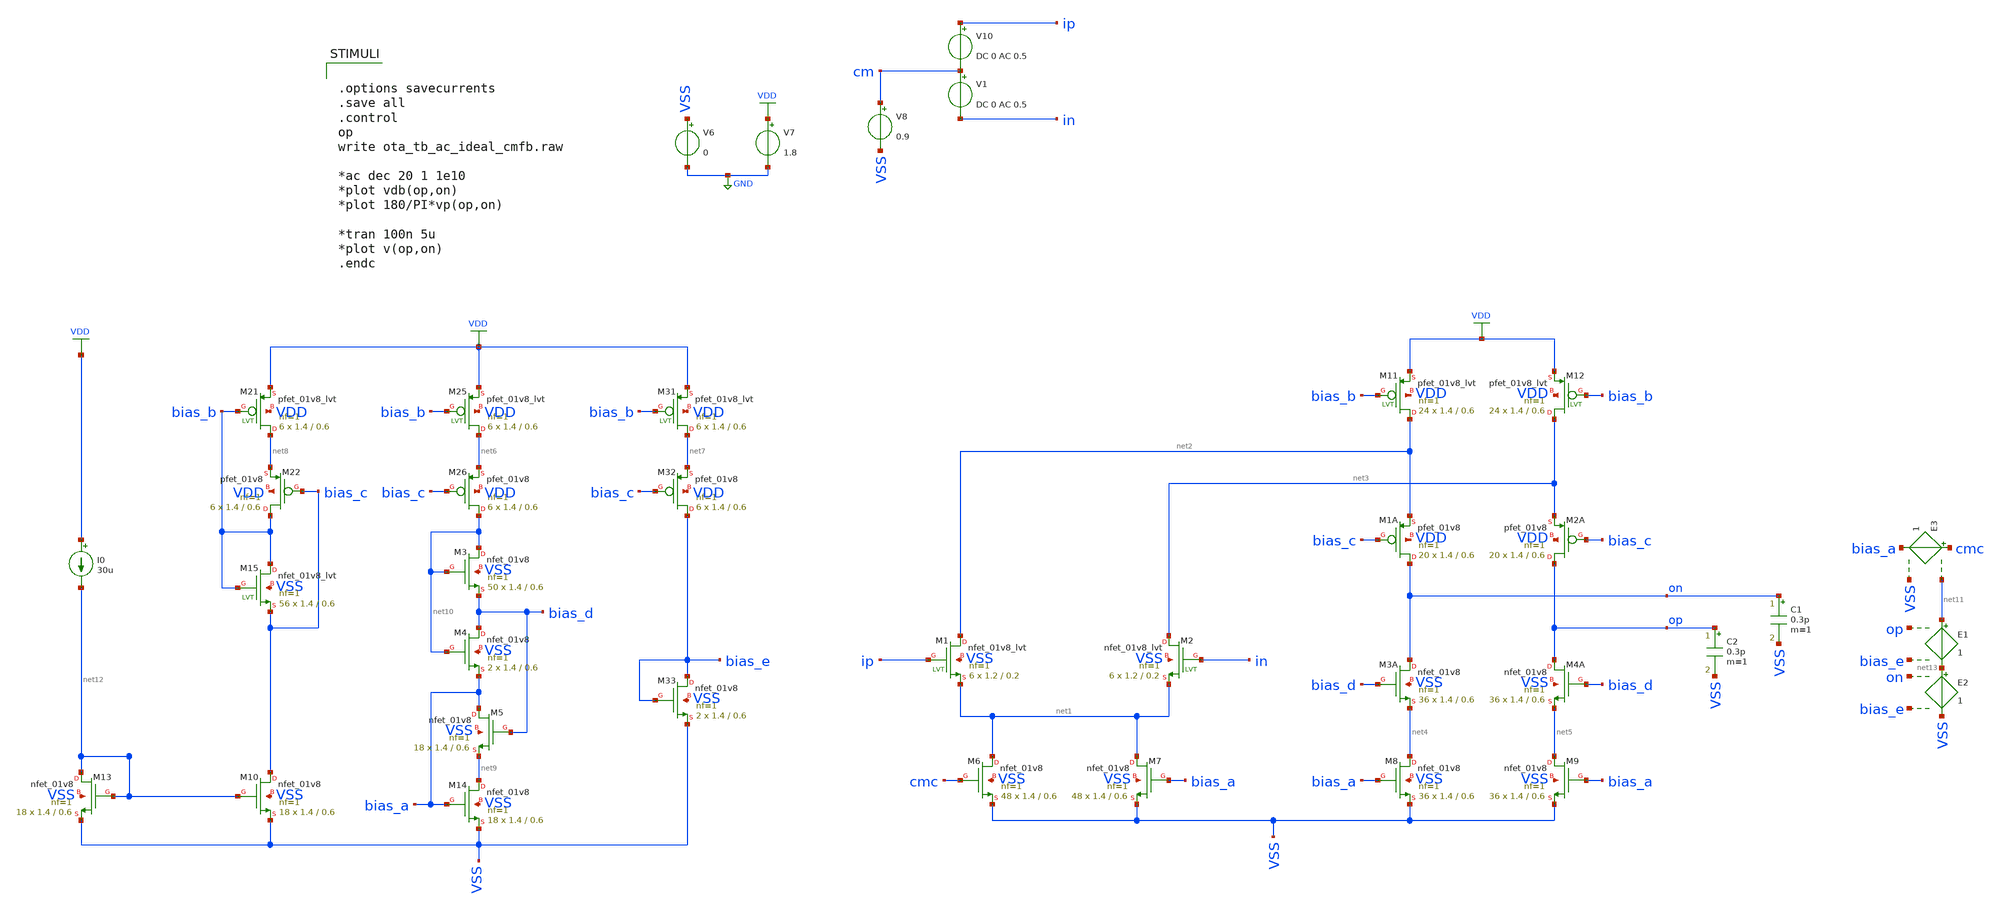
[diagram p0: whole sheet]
** sch_path: verification/schematic/folded_cascode_tb.sch
**.subckt folded_cascode_tb
XM1 net2 ip net1 VSS sky130_fd_pr__nfet_01v8_lvt L=0.2 W=1.2 nf=1 ad='int((nf+1)/2) * W/nf * 0.29' as='int((nf+2)/2) * W/nf * 0.29'
+ pd='2*int((nf+1)/2) * (W/nf + 0.29)' ps='2*int((nf+2)/2) * (W/nf + 0.29)' nrd='0.29 / W' nrs='0.29 / W'
+ sa=0 sb=0 sd=0 mult=6 m=6
XM2 net3 in net1 VSS sky130_fd_pr__nfet_01v8_lvt L=0.2 W=1.2 nf=1 ad='int((nf+1)/2) * W/nf * 0.29' as='int((nf+2)/2) * W/nf * 0.29'
+ pd='2*int((nf+1)/2) * (W/nf + 0.29)' ps='2*int((nf+2)/2) * (W/nf + 0.29)' nrd='0.29 / W' nrs='0.29 / W'
+ sa=0 sb=0 sd=0 mult=6 m=6
XM6 net1 cmc VSS VSS sky130_fd_pr__nfet_01v8 L=0.6 W=1.4 nf=1 ad='int((nf+1)/2) * W/nf * 0.29' as='int((nf+2)/2) * W/nf * 0.29'
+ pd='2*int((nf+1)/2) * (W/nf + 0.29)' ps='2*int((nf+2)/2) * (W/nf + 0.29)' nrd='0.29 / W' nrs='0.29 / W'
+ sa=0 sb=0 sd=0 mult=48 m=48
XM7 net1 bias_a VSS VSS sky130_fd_pr__nfet_01v8 L=0.6 W=1.4 nf=1 ad='int((nf+1)/2) * W/nf * 0.29' as='int((nf+2)/2) * W/nf * 0.29'
+ pd='2*int((nf+1)/2) * (W/nf + 0.29)' ps='2*int((nf+2)/2) * (W/nf + 0.29)' nrd='0.29 / W' nrs='0.29 / W'
+ sa=0 sb=0 sd=0 mult=48 m=48
XM11 net2 bias_b VDD VDD sky130_fd_pr__pfet_01v8_lvt L=0.6 W=1.4 nf=1 ad='int((nf+1)/2) * W/nf * 0.29'
+ as='int((nf+2)/2) * W/nf * 0.29' pd='2*int((nf+1)/2) * (W/nf + 0.29)' ps='2*int((nf+2)/2) * (W/nf + 0.29)'
+ nrd='0.29 / W' nrs='0.29 / W' sa=0 sb=0 sd=0 mult=24 m=24
XM12 net3 bias_b VDD VDD sky130_fd_pr__pfet_01v8_lvt L=0.6 W=1.4 nf=1 ad='int((nf+1)/2) * W/nf * 0.29'
+ as='int((nf+2)/2) * W/nf * 0.29' pd='2*int((nf+1)/2) * (W/nf + 0.29)' ps='2*int((nf+2)/2) * (W/nf + 0.29)'
+ nrd='0.29 / W' nrs='0.29 / W' sa=0 sb=0 sd=0 mult=24 m=24
XM1A on bias_c net2 VDD sky130_fd_pr__pfet_01v8 L=0.6 W=1.4 nf=1 ad='int((nf+1)/2) * W/nf * 0.29' as='int((nf+2)/2) * W/nf * 0.29'
+ pd='2*int((nf+1)/2) * (W/nf + 0.29)' ps='2*int((nf+2)/2) * (W/nf + 0.29)' nrd='0.29 / W' nrs='0.29 / W'
+ sa=0 sb=0 sd=0 mult=20 m=20
XM2A op bias_c net3 VDD sky130_fd_pr__pfet_01v8 L=0.6 W=1.4 nf=1 ad='int((nf+1)/2) * W/nf * 0.29' as='int((nf+2)/2) * W/nf * 0.29'
+ pd='2*int((nf+1)/2) * (W/nf + 0.29)' ps='2*int((nf+2)/2) * (W/nf + 0.29)' nrd='0.29 / W' nrs='0.29 / W'
+ sa=0 sb=0 sd=0 mult=20 m=20
XM3A on bias_d net4 VSS sky130_fd_pr__nfet_01v8 L=0.6 W=1.4 nf=1 ad='int((nf+1)/2) * W/nf * 0.29' as='int((nf+2)/2) * W/nf * 0.29'
+ pd='2*int((nf+1)/2) * (W/nf + 0.29)' ps='2*int((nf+2)/2) * (W/nf + 0.29)' nrd='0.29 / W' nrs='0.29 / W'
+ sa=0 sb=0 sd=0 mult=36 m=36
XM4A op bias_d net5 VSS sky130_fd_pr__nfet_01v8 L=0.6 W=1.4 nf=1 ad='int((nf+1)/2) * W/nf * 0.29' as='int((nf+2)/2) * W/nf * 0.29'
+ pd='2*int((nf+1)/2) * (W/nf + 0.29)' ps='2*int((nf+2)/2) * (W/nf + 0.29)' nrd='0.29 / W' nrs='0.29 / W'
+ sa=0 sb=0 sd=0 mult=36 m=36
XM8 net4 bias_a VSS VSS sky130_fd_pr__nfet_01v8 L=0.6 W=1.4 nf=1 ad='int((nf+1)/2) * W/nf * 0.29' as='int((nf+2)/2) * W/nf * 0.29'
+ pd='2*int((nf+1)/2) * (W/nf + 0.29)' ps='2*int((nf+2)/2) * (W/nf + 0.29)' nrd='0.29 / W' nrs='0.29 / W'
+ sa=0 sb=0 sd=0 mult=36 m=36
XM9 net5 bias_a VSS VSS sky130_fd_pr__nfet_01v8 L=0.6 W=1.4 nf=1 ad='int((nf+1)/2) * W/nf * 0.29' as='int((nf+2)/2) * W/nf * 0.29'
+ pd='2*int((nf+1)/2) * (W/nf + 0.29)' ps='2*int((nf+2)/2) * (W/nf + 0.29)' nrd='0.29 / W' nrs='0.29 / W'
+ sa=0 sb=0 sd=0 mult=36 m=36
V6 VSS GND 0
V7 VDD GND 1.8
V8 cm VSS 0.9
V10 ip cm DC 0 AC 0.5
V1 cm in DC 0 AC 0.5
XM22 bias_b bias_c net8 VDD sky130_fd_pr__pfet_01v8 L=0.6 W=1.4 nf=1 ad='int((nf+1)/2) * W/nf * 0.29'
+ as='int((nf+2)/2) * W/nf * 0.29' pd='2*int((nf+1)/2) * (W/nf + 0.29)' ps='2*int((nf+2)/2) * (W/nf + 0.29)'
+ nrd='0.29 / W' nrs='0.29 / W' sa=0 sb=0 sd=0 mult=6 m=6
XM26 net10 bias_c net6 VDD sky130_fd_pr__pfet_01v8 L=0.6 W=1.4 nf=1 ad='int((nf+1)/2) * W/nf * 0.29'
+ as='int((nf+2)/2) * W/nf * 0.29' pd='2*int((nf+1)/2) * (W/nf + 0.29)' ps='2*int((nf+2)/2) * (W/nf + 0.29)'
+ nrd='0.29 / W' nrs='0.29 / W' sa=0 sb=0 sd=0 mult=6 m=6
XM32 bias_e bias_c net7 VDD sky130_fd_pr__pfet_01v8 L=0.6 W=1.4 nf=1 ad='int((nf+1)/2) * W/nf * 0.29'
+ as='int((nf+2)/2) * W/nf * 0.29' pd='2*int((nf+1)/2) * (W/nf + 0.29)' ps='2*int((nf+2)/2) * (W/nf + 0.29)'
+ nrd='0.29 / W' nrs='0.29 / W' sa=0 sb=0 sd=0 mult=6 m=6
XM33 bias_e bias_e VSS VSS sky130_fd_pr__nfet_01v8 L=0.6 W=1.4 nf=1 ad='int((nf+1)/2) * W/nf * 0.29'
+ as='int((nf+2)/2) * W/nf * 0.29' pd='2*int((nf+1)/2) * (W/nf + 0.29)' ps='2*int((nf+2)/2) * (W/nf + 0.29)'
+ nrd='0.29 / W' nrs='0.29 / W' sa=0 sb=0 sd=0 mult=2 m=2
XM21 net8 bias_b VDD VDD sky130_fd_pr__pfet_01v8_lvt L=0.6 W=1.4 nf=1 ad='int((nf+1)/2) * W/nf * 0.29'
+ as='int((nf+2)/2) * W/nf * 0.29' pd='2*int((nf+1)/2) * (W/nf + 0.29)' ps='2*int((nf+2)/2) * (W/nf + 0.29)'
+ nrd='0.29 / W' nrs='0.29 / W' sa=0 sb=0 sd=0 mult=6 m=6
XM25 net6 bias_b VDD VDD sky130_fd_pr__pfet_01v8_lvt L=0.6 W=1.4 nf=1 ad='int((nf+1)/2) * W/nf * 0.29'
+ as='int((nf+2)/2) * W/nf * 0.29' pd='2*int((nf+1)/2) * (W/nf + 0.29)' ps='2*int((nf+2)/2) * (W/nf + 0.29)'
+ nrd='0.29 / W' nrs='0.29 / W' sa=0 sb=0 sd=0 mult=6 m=6
XM31 net7 bias_b VDD VDD sky130_fd_pr__pfet_01v8_lvt L=0.6 W=1.4 nf=1 ad='int((nf+1)/2) * W/nf * 0.29'
+ as='int((nf+2)/2) * W/nf * 0.29' pd='2*int((nf+1)/2) * (W/nf + 0.29)' ps='2*int((nf+2)/2) * (W/nf + 0.29)'
+ nrd='0.29 / W' nrs='0.29 / W' sa=0 sb=0 sd=0 mult=6 m=6
XM3 net10 net10 bias_d VSS sky130_fd_pr__nfet_01v8 L=0.6 W=1.4 nf=1 ad='int((nf+1)/2) * W/nf * 0.29'
+ as='int((nf+2)/2) * W/nf * 0.29' pd='2*int((nf+1)/2) * (W/nf + 0.29)' ps='2*int((nf+2)/2) * (W/nf + 0.29)'
+ nrd='0.29 / W' nrs='0.29 / W' sa=0 sb=0 sd=0 mult=50 m=50
XM4 bias_d net10 bias_a VSS sky130_fd_pr__nfet_01v8 L=0.6 W=1.4 nf=1 ad='int((nf+1)/2) * W/nf * 0.29'
+ as='int((nf+2)/2) * W/nf * 0.29' pd='2*int((nf+1)/2) * (W/nf + 0.29)' ps='2*int((nf+2)/2) * (W/nf + 0.29)'
+ nrd='0.29 / W' nrs='0.29 / W' sa=0 sb=0 sd=0 mult=2 m=2
XM5 bias_a bias_d net9 VSS sky130_fd_pr__nfet_01v8 L=0.6 W=1.4 nf=1 ad='int((nf+1)/2) * W/nf * 0.29'
+ as='int((nf+2)/2) * W/nf * 0.29' pd='2*int((nf+1)/2) * (W/nf + 0.29)' ps='2*int((nf+2)/2) * (W/nf + 0.29)'
+ nrd='0.29 / W' nrs='0.29 / W' sa=0 sb=0 sd=0 mult=18 m=18
XM14 net9 bias_a VSS VSS sky130_fd_pr__nfet_01v8 L=0.6 W=1.4 nf=1 ad='int((nf+1)/2) * W/nf * 0.29' as='int((nf+2)/2) * W/nf * 0.29'
+ pd='2*int((nf+1)/2) * (W/nf + 0.29)' ps='2*int((nf+2)/2) * (W/nf + 0.29)' nrd='0.29 / W' nrs='0.29 / W'
+ sa=0 sb=0 sd=0 mult=18 m=18
XM15 bias_b bias_b bias_c VSS sky130_fd_pr__nfet_01v8_lvt L=0.6 W=1.4 nf=1 ad='int((nf+1)/2) * W/nf * 0.29'
+ as='int((nf+2)/2) * W/nf * 0.29' pd='2*int((nf+1)/2) * (W/nf + 0.29)' ps='2*int((nf+2)/2) * (W/nf + 0.29)'
+ nrd='0.29 / W' nrs='0.29 / W' sa=0 sb=0 sd=0 mult=56 m=56
E1 net11 net13 op bias_e 1
E2 net13 VSS on bias_e 1
E3 cmc bias_a net11 VSS 1
C1 on VSS 0.3p m=1
C2 op VSS 0.3p m=1
XM10 bias_c net12 VSS VSS sky130_fd_pr__nfet_01v8 L=0.6 W=1.4 nf=1 ad='int((nf+1)/2) * W/nf * 0.29' as='int((nf+2)/2) * W/nf * 0.29'
+ pd='2*int((nf+1)/2) * (W/nf + 0.29)' ps='2*int((nf+2)/2) * (W/nf + 0.29)' nrd='0.29 / W' nrs='0.29 / W'
+ sa=0 sb=0 sd=0 mult=18 m=18
XM13 net12 net12 VSS VSS sky130_fd_pr__nfet_01v8 L=0.6 W=1.4 nf=1 ad='int((nf+1)/2) * W/nf * 0.29' as='int((nf+2)/2) * W/nf * 0.29'
+ pd='2*int((nf+1)/2) * (W/nf + 0.29)' ps='2*int((nf+2)/2) * (W/nf + 0.29)' nrd='0.29 / W' nrs='0.29 / W'
+ sa=0 sb=0 sd=0 mult=18 m=18
I0 VDD net12 30u
**** begin user architecture code

** opencircuitdesign pdks install
.lib /farmshare/home/classes/ee/372/PDKs/open_pdks_1.0.310/sky130/sky130A/libs.tech/ngspice/sky130.lib.spice tt



.options savecurrents
.save all
.control
op
write ota_tb_ac_ideal_cmfb.raw

*ac dec 20 1 1e10
*plot vdb(op,on)
*plot 180/PI*vp(op,on)

*tran 100n 5u
*plot v(op,on)
.endc


**** end user architecture code
**.ends
.GLOBAL VDD
.GLOBAL GND
.end
